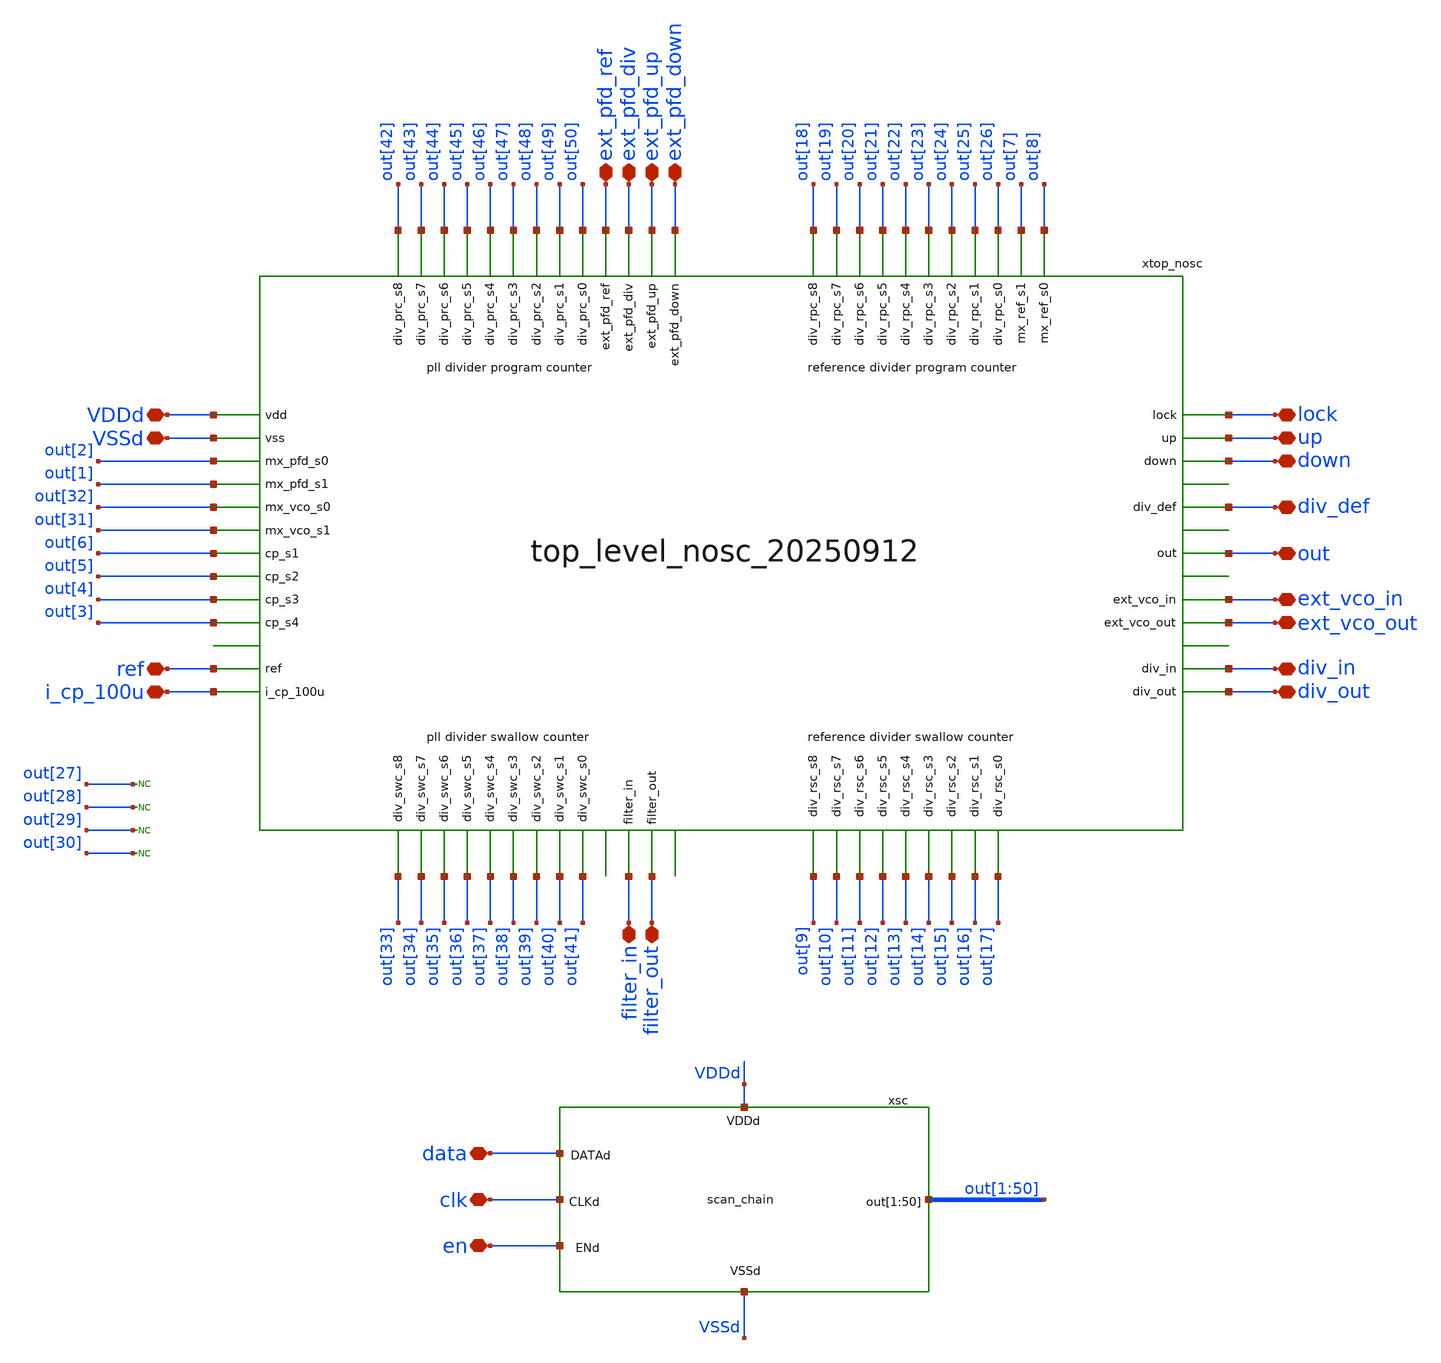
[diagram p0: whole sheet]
** sch_path: designs/libs/top_level/top_level_20250912/top_level_20250912_sc/top_level_20250912_sc.sch
**.subckt top_level_20250912_sc VDDd VSSd ref i_cp_100u filter_in filter_out ext_pfd_ref ext_pfd_up
*+ ext_pfd_down ext_pfd_div up down out lock ext_vco_out ext_vco_in div_out div_in div_def data clk en
*.iopin VDDd
*.iopin VSSd
*.iopin ref
*.iopin i_cp_100u
*.iopin filter_in
*.iopin filter_out
*.iopin ext_pfd_ref
*.iopin ext_pfd_up
*.iopin ext_pfd_down
*.iopin ext_pfd_div
*.iopin up
*.iopin down
*.iopin out
*.iopin lock
*.iopin ext_vco_out
*.iopin ext_vco_in
*.iopin div_out
*.iopin div_in
*.iopin div_def
*.iopin data
*.iopin clk
*.iopin en
xtop_nosc VDDd VSSd out[2] out[1] out[32] out[31] out[33] out[6] out[5] out[4] out[3] out[34]
+ out[35] out[36] out[37] out[38] out[39] out[40] out[41] out[42] out[43] out[44] out[45] out[46] out[47]
+ out[48] out[49] out[50] ref i_cp_100u ext_pfd_ref ext_pfd_div ext_pfd_up ext_pfd_down lock up down
+ filter_out ext_vco_in div_in div_out out filter_in ext_vco_out div_def out[18] out[19] out[20] out[21] out[22]
+ out[23] out[24] out[25] out[26] out[7] out[8] out[9] out[10] out[11] out[12] out[13] out[14] out[15]
+ out[16] out[17] top_level_20250912_nosc
* noconn out[27]
* noconn out[28]
* noconn out[29]
* noconn out[30]
xsc VDDd VSSd clk en data out[1] out[2] out[3] out[4] out[5] out[6] out[7] out[8] out[9] out[10]
+ out[11] out[12] out[13] out[14] out[15] out[16] out[17] out[18] out[19] out[20] out[21] out[22] out[23]
+ out[24] out[25] out[26] out[27] out[28] out[29] out[30] out[31] out[32] out[33] out[34] out[35] out[36]
+ out[37] out[38] out[39] out[40] out[41] out[42] out[43] out[44] out[45] out[46] out[47] out[48] out[49]
+ out[50] scan_chain
**.ends
.end
